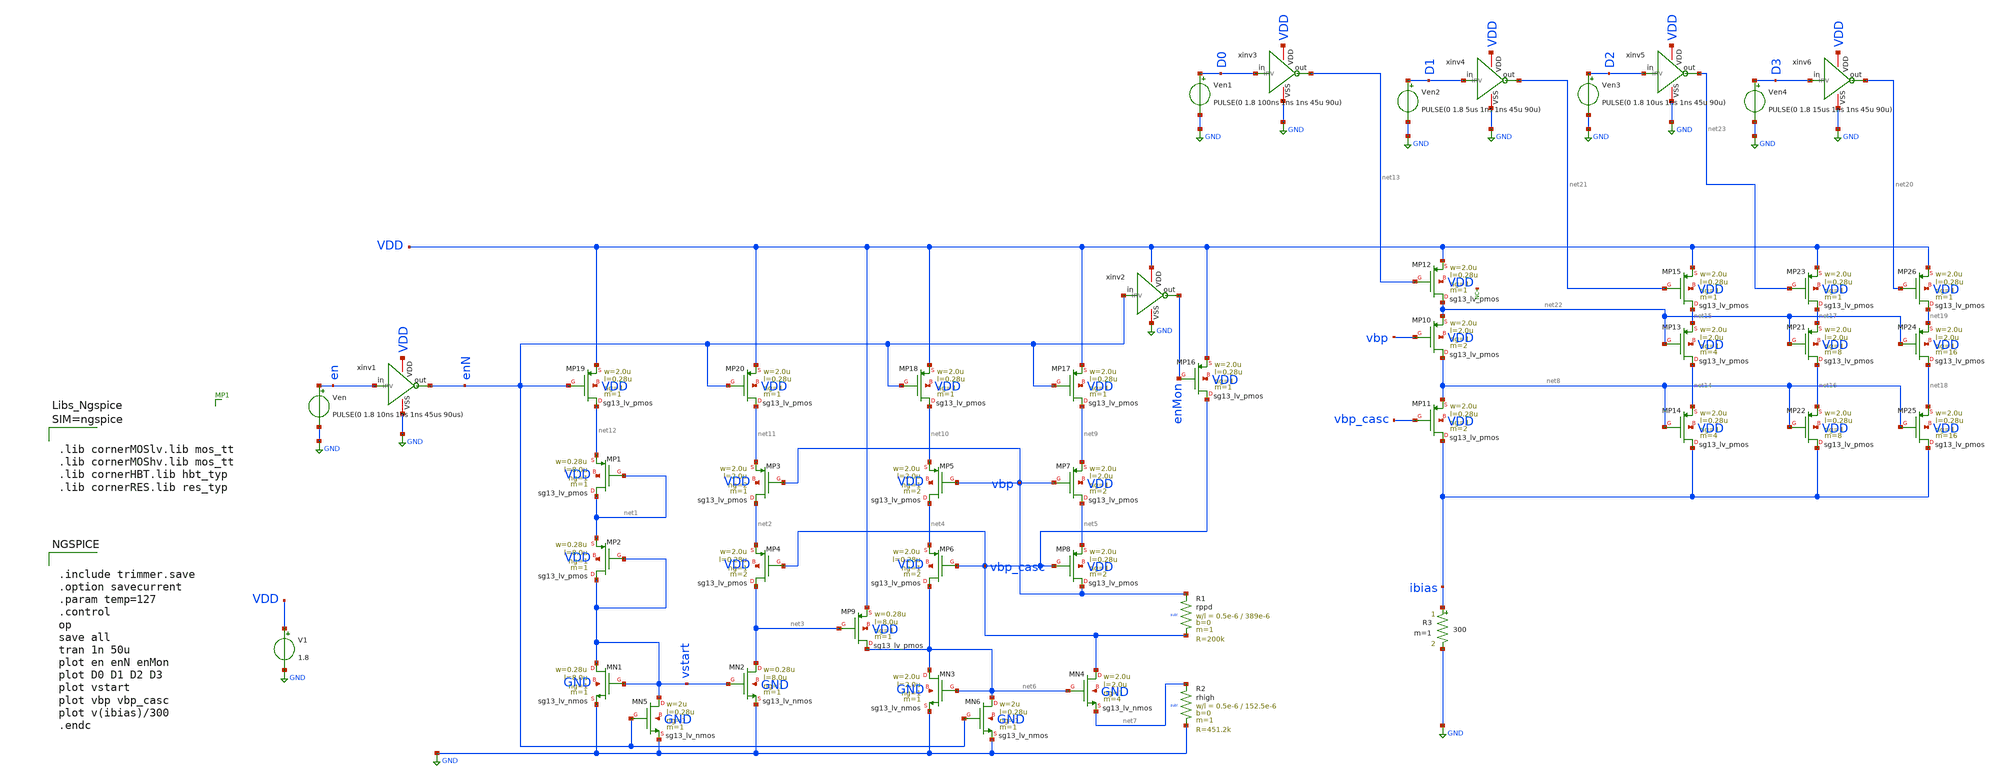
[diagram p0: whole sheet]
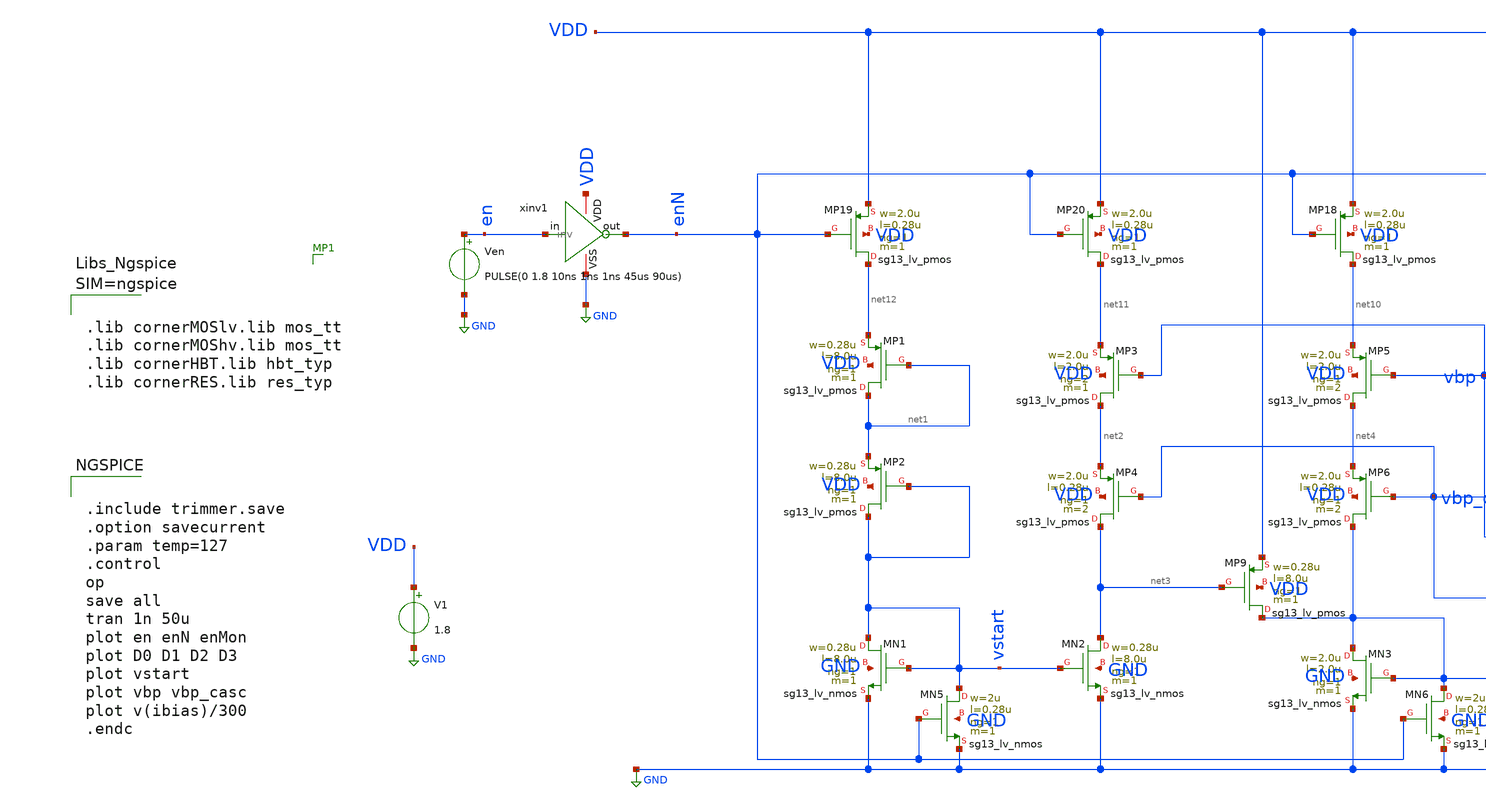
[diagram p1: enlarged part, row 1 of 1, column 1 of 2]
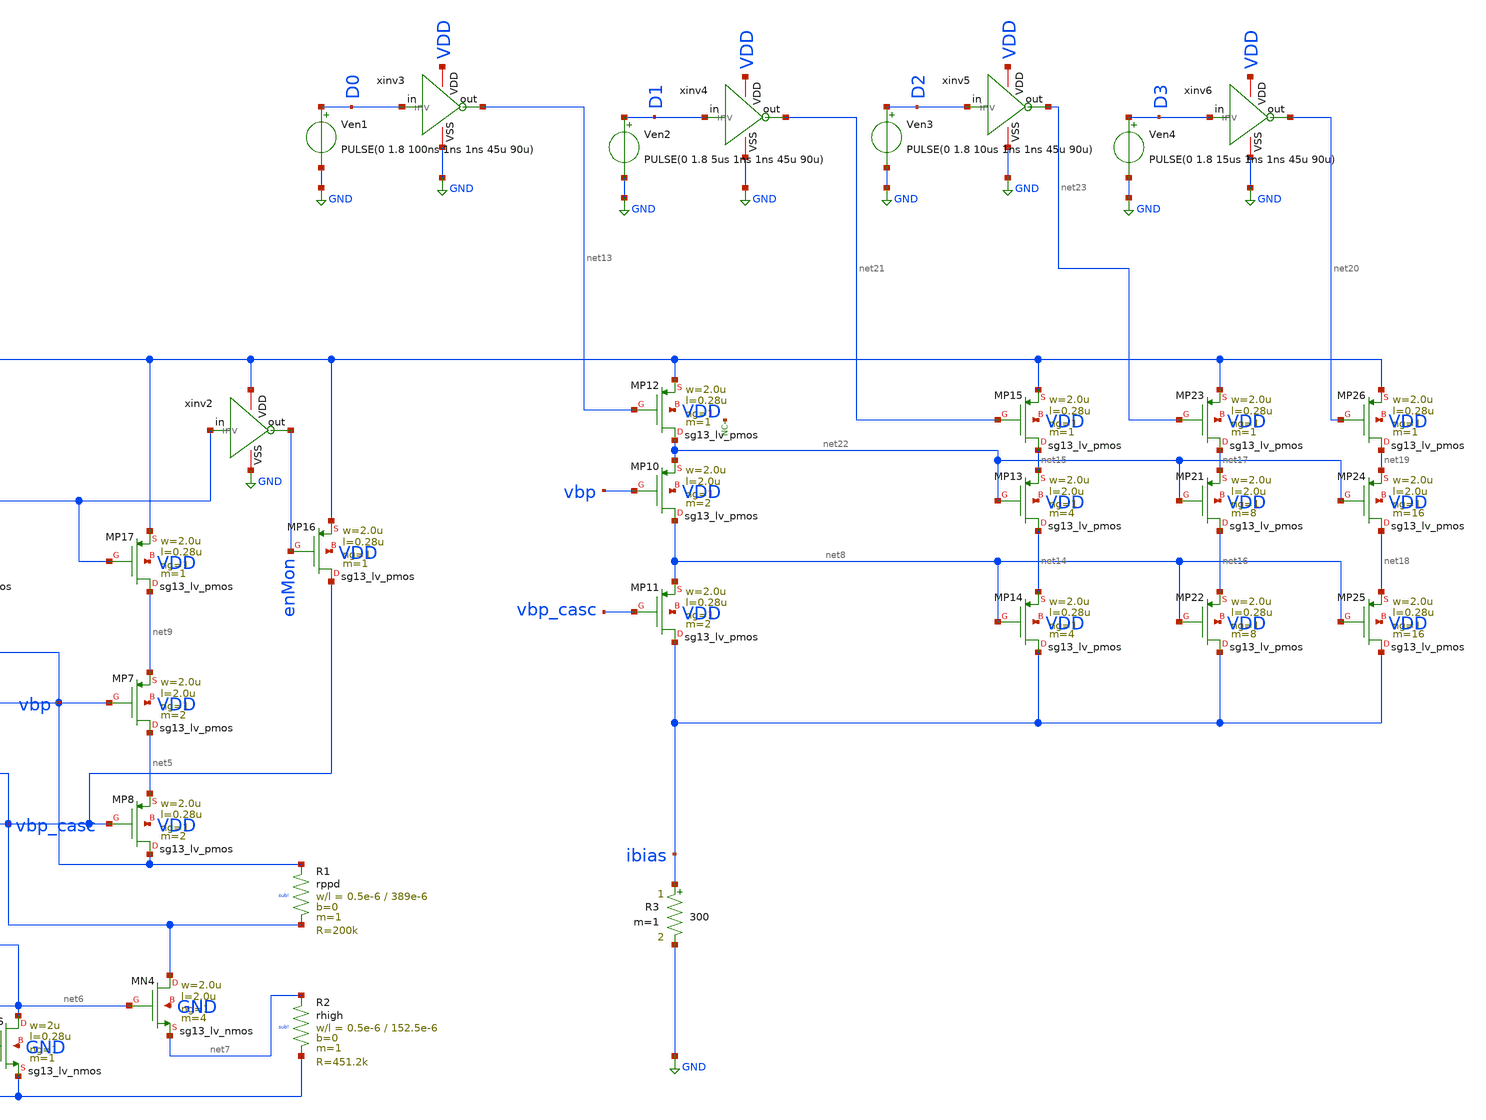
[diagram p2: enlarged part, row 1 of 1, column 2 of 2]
** sch_path: blocks/composite/dpi_adexp_neuron/design_data/xschem/trimmer_test.sch
**.subckt trimmer_test
XMP1 net1 net1 net12 VDD sg13_lv_pmos w=0.28u l=8.0u ng=1 m=1 mm_ok=1
XMP2 vstart vstart net1 VDD sg13_lv_pmos w=0.28u l=8.0u ng=1 m=1 mm_ok=1
XMN2 net3 vstart GND GND sg13_lv_nmos w=0.28u l=8.0u ng=1 m=1 mm_ok=1
XMN1 vstart vstart GND GND sg13_lv_nmos w=0.28u l=8.0u ng=1 m=1 mm_ok=1
XMP3 net2 vbp net11 VDD sg13_lv_pmos w=2.0u l=2.0u ng=2 m=1 mm_ok=1
XMP4 net3 vbp_casc net2 VDD sg13_lv_pmos w=2.0u l=0.28u ng=1 m=2 mm_ok=1
XMP5 net4 vbp net10 VDD sg13_lv_pmos w=2.0u l=2.0u ng=1 m=2 mm_ok=1
XMP6 net6 vbp_casc net4 VDD sg13_lv_pmos w=2.0u l=0.28u ng=1 m=2 mm_ok=1
XMP7 net5 vbp net9 VDD sg13_lv_pmos w=2.0u l=2.0u ng=1 m=2 mm_ok=1
XMP8 vbp vbp_casc net5 VDD sg13_lv_pmos w=2.0u l=0.28u ng=1 m=2 mm_ok=1
XMP9 net6 net3 VDD VDD sg13_lv_pmos w=0.28u l=8.0u ng=1 m=1 mm_ok=1
XMN3 net6 net6 GND GND sg13_lv_nmos w=2.0u l=2.0u ng=1 m=1 mm_ok=1
XMN4 vbp_casc net6 net7 GND sg13_lv_nmos w=2.0u l=2.0u ng=1 m=4 mm_ok=1
XR1 vbp vbp_casc sub! rppd w=0.5e-6 l=389e-6 m=1 b=0 mm_ok=1
XR2 net7 GND sub! rhigh w=0.5e-6 l=152.5e-6 m=1 b=0 mm_ok=1
R3 ibias GND 300 m=1
XMP10 net8 vbp net22 VDD sg13_lv_pmos w=2.0u l=2.0u ng=1 m=2 mm_ok=1
XMP11 ibias vbp_casc net8 VDD sg13_lv_pmos w=2.0u l=0.28u ng=1 m=2 mm_ok=1
XMP16 vbp_casc enMon VDD VDD sg13_lv_pmos w=2.0u l=0.28u ng=1 m=1 mm_ok=1
XMP17 net9 enN VDD VDD sg13_lv_pmos w=2.0u l=0.28u ng=1 m=1 mm_ok=1
XMP18 net10 enN VDD VDD sg13_lv_pmos w=2.0u l=0.28u ng=1 m=1 mm_ok=1
XMP19 net12 enN VDD VDD sg13_lv_pmos w=2.0u l=0.28u ng=1 m=1 mm_ok=1
XMP20 net11 enN VDD VDD sg13_lv_pmos w=2.0u l=0.28u ng=1 m=1 mm_ok=1
XMN5 vstart enN GND GND sg13_lv_nmos w=2u l=0.28u ng=1 m=1 mm_ok=1
XMN6 net6 enN GND GND sg13_lv_nmos w=2u l=0.28u ng=1 m=1 mm_ok=1
V1 VDD GND 1.8
Ven en GND PULSE(0 1.8 10ns 1ns 1ns 45us 90us)
xinv1 VDD en enN GND inv
xinv2 VDD enN enMon GND inv
XMP12 net22 net13 VDD VDD sg13_lv_pmos w=2.0u l=0.28u ng=1 m=1 mm_ok=1
Ven1 D0 GND PULSE(0 1.8 100ns 1ns 1ns 45u 90u)

xinv3 VDD D0 net13 GND inv
XMP13 net14 net22 net15 VDD sg13_lv_pmos w=2.0u l=2.0u ng=1 m=4 mm_ok=1
XMP14 ibias net8 net14 VDD sg13_lv_pmos w=2.0u l=0.28u ng=1 m=4 mm_ok=1
XMP15 net15 net21 VDD VDD sg13_lv_pmos w=2.0u l=0.28u ng=1 m=1 mm_ok=1
XMP21 net16 net22 net17 VDD sg13_lv_pmos w=2.0u l=2.0u ng=1 m=8 mm_ok=1
XMP22 ibias net8 net16 VDD sg13_lv_pmos w=2.0u l=0.28u ng=1 m=8 mm_ok=1
XMP23 net17 net23 VDD VDD sg13_lv_pmos w=2.0u l=0.28u ng=1 m=1 mm_ok=1
XMP24 net18 net22 net19 VDD sg13_lv_pmos w=2.0u l=2.0u ng=1 m=16 mm_ok=1
XMP25 ibias net8 net18 VDD sg13_lv_pmos w=2.0u l=0.28u ng=1 m=16 mm_ok=1
XMP26 net19 net20 VDD VDD sg13_lv_pmos w=2.0u l=0.28u ng=1 m=1 mm_ok=1
Ven2 D1 GND PULSE(0 1.8 5us 1ns 1ns 45u 90u)

xinv4 VDD D1 net21 GND inv
Ven3 D2 GND PULSE(0 1.8 10us 1ns 1ns 45u 90u)

xinv5 VDD D2 net23 GND inv
Ven4 D3 GND PULSE(0 1.8 15us 1ns 1ns 45u 90u)

xinv6 VDD D3 net20 GND inv
* noconn #net24
**** begin user architecture code


.include trimmer.save
.option savecurrent
.param temp=127
.control
op
save all
tran 1n 50u
plot en enN enMon
plot D0 D1 D2 D3
plot vstart
plot vbp vbp_casc
plot v(ibias)/300
.endc





.lib cornerMOSlv.lib mos_tt
.lib cornerMOShv.lib mos_tt
.lib cornerHBT.lib hbt_typ
.lib cornerRES.lib res_typ



**** end user architecture code
**.ends

* expanding   symbol:  inv.sym # of pins=4
** sym_path: blocks/composite/dpi_adexp_neuron/design_data/xschem/dev/inv.sym
** sch_path: blocks/composite/dpi_adexp_neuron/design_data/xschem/dev/inv.sch
.subckt inv VDD in out VSS
*.iopin VDD
*.ipin in
*.iopin VSS
*.opin out
XM1 out in VSS VSS sg13_lv_nmos w=2.0u l=0.28u ng=1 m=1 mm_ok=1
XM2 out in VDD VDD sg13_lv_pmos w=2.0u l=0.28u ng=1 m=1 mm_ok=1
.ends

.GLOBAL GND
.end
